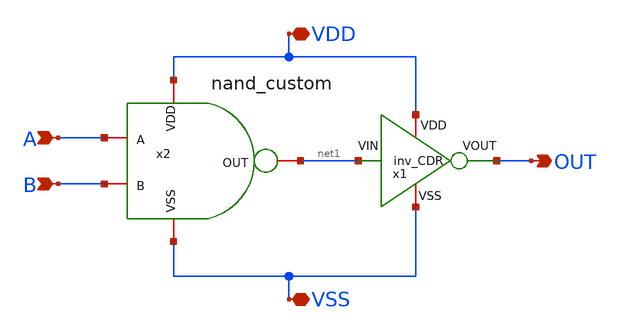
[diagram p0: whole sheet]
** sch_path: CDR4176-main/schematic/xschem/and_custom/and_custom.sch
**.subckt and_custom A VDD OUT VSS B
*.ipin A
*.iopin VDD
*.opin OUT
*.iopin VSS
*.ipin B
x1 VDD OUT net1 VSS inv_CDR
x2 VDD net1 A B VSS nand_custom
**.ends

* expanding   symbol:  inv_CDR/inv_CDR.sym # of pins=4
** sym_path: CDR4176-main/schematic/xschem/inv_CDR/inv_CDR.sym
** sch_path: CDR4176-main/schematic/xschem/inv_CDR/inv_CDR.sch
.subckt inv_CDR VDD VOUT VIN VSS
*.iopin VDD
*.iopin VSS
*.opin VOUT
*.ipin VIN
XM2 VOUT VIN VDD VDD sg13_lv_pmos w=0.15u l=0.13u ng=1 m=1 mm_ok=1
XM1 VOUT VIN VSS VSS sg13_lv_nmos w=0.15u l=0.13u ng=1 m=1 mm_ok=1
.ends


* expanding   symbol:  nand_custom/nand_custom.sym # of pins=5
** sym_path: CDR4176-main/schematic/xschem/nand_custom/nand_custom.sym
** sch_path: CDR4176-main/schematic/xschem/nand_custom/nand_custom.sch
.subckt nand_custom VDD OUT A B VSS
*.iopin VDD
*.iopin VSS
*.ipin A
*.ipin B
*.opin OUT
XM1 OUT A net1 VSS sg13_lv_nmos w=0.15u l=0.13u ng=1 m=1 mm_ok=1
XM2 OUT A VDD VDD sg13_lv_pmos w=0.15u l=0.13u ng=1 m=1 mm_ok=1
XM3 net1 B VSS VSS sg13_lv_nmos w=0.15u l=0.13u ng=1 m=1 mm_ok=1
XM4 OUT B VDD VDD sg13_lv_pmos w=0.15u l=0.13u ng=1 m=1 mm_ok=1
.ends

.end
